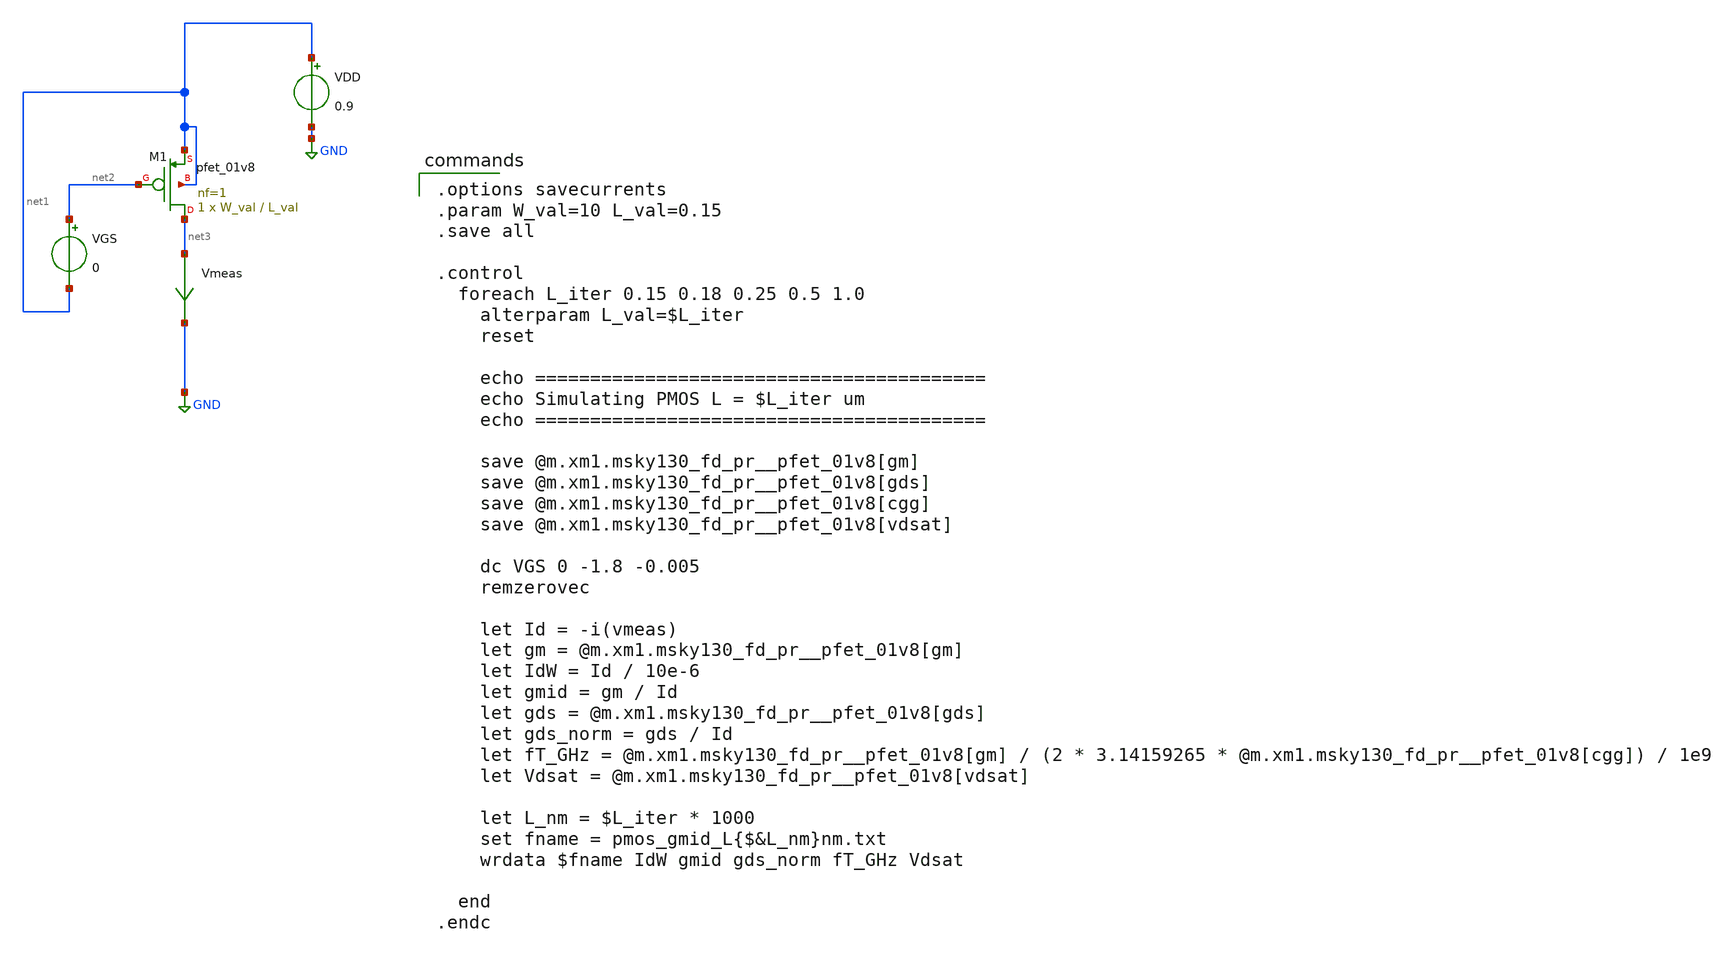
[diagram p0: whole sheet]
** sch_path: 01_xschem_ngspice/soluzioni/lab02/xschem/pmos_gmid.sch
**.subckt pmos_gmid
XM1 net3 net2 net1 net1 sky130_fd_pr__pfet_01v8 L=L_val W=W_val nf=1 ad='int((1 + 1)/2) * W_val / 1 * 0.29'
+ as='int((1 + 2)/2) * W_val / 1 * 0.29' pd='2*int((1 + 1)/2) * (W_val / 1 + 0.29)' ps='2*int((1 + 2)/2) * (W_val / 1 + 0.29)'
+ nrd='0.29 / W_val ' nrs='0.29 / W_val ' sa=0 sb=0 sd=0 mult=1 m=1
VDD net1 GND 0.9
VGS net2 net1 0
Vmeas net3 GND 0
.save i(vmeas)
**** begin user architecture code

** opencircuitdesign pdks install
.lib $::SKYWATER_MODELS/sky130.lib.spice tt


.options savecurrents
.param W_val=10 L_val=0.15
.save all

.control
  foreach L_iter 0.15 0.18 0.25 0.5 1.0
    alterparam L_val=$L_iter
    reset

    echo =========================================
    echo Simulating PMOS L = $L_iter um
    echo =========================================

    save @m.xm1.msky130_fd_pr__pfet_01v8[gm]
    save @m.xm1.msky130_fd_pr__pfet_01v8[gds]
    save @m.xm1.msky130_fd_pr__pfet_01v8[cgg]
    save @m.xm1.msky130_fd_pr__pfet_01v8[vdsat]

    dc VGS 0 -1.8 -0.005
    remzerovec

    let Id = -i(vmeas)
    let gm = @m.xm1.msky130_fd_pr__pfet_01v8[gm]
    let IdW = Id / 10e-6
    let gmid = gm / Id
    let gds = @m.xm1.msky130_fd_pr__pfet_01v8[gds]
    let gds_norm = gds / Id
    let fT_GHz = @m.xm1.msky130_fd_pr__pfet_01v8[gm] / (2 * 3.14159265 *
+ @m.xm1.msky130_fd_pr__pfet_01v8[cgg]) / 1e9
    let Vdsat = @m.xm1.msky130_fd_pr__pfet_01v8[vdsat]

    let L_nm = $L_iter * 1000
    set fname = pmos_gmid_L{$&L_nm}nm.txt
    wrdata $fname IdW gmid gds_norm fT_GHz Vdsat

  end
.endc

**** end user architecture code
**.ends
.GLOBAL GND
.end
